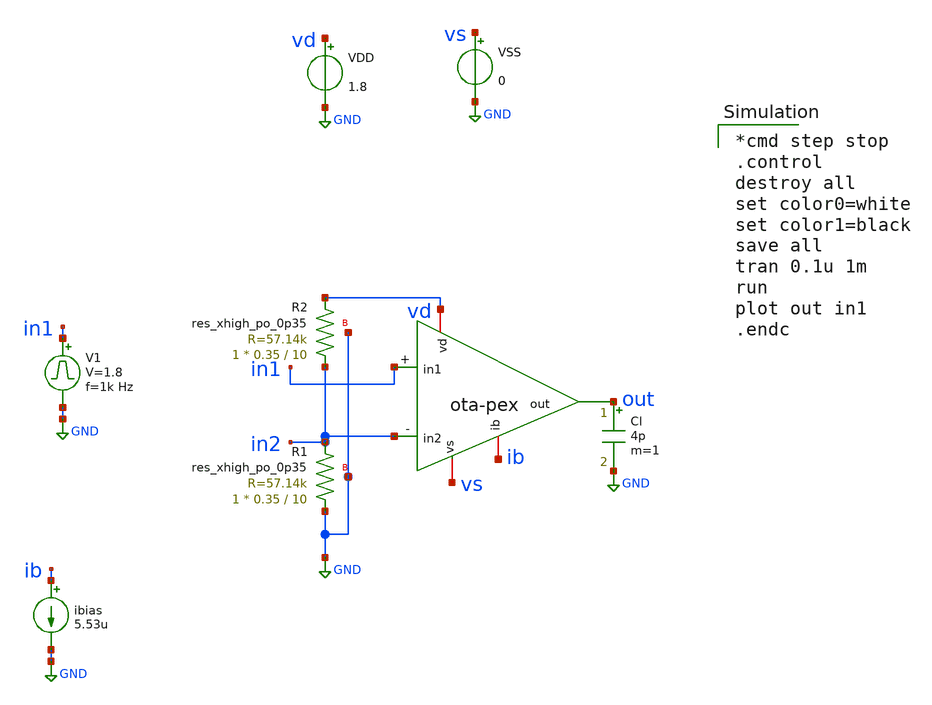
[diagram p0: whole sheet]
** sch_path: ota/xschem/ota_tb-largesignal.sch
* Copyright 2020 Stefan Frederik Schippers
* Licensed under the Apache License, Version 2.0 (the "License");
* you may not use this file except in compliance with the License.
* You may obtain a copy of the License at
* https://www.apache.org/licenses/LICENSE-2.0
* Unless required by applicable law or agreed to in writing, software
* distributed under the License is distributed on an "AS IS" BASIS,
* WITHOUT WARRANTIES OR CONDITIONS OF ANY KIND, either express or implied.
* See the License for the specific language governing permissions and
* limitations under the License.
**.subckt ota_tb-largesignal
ibias ib GND 5.53u
VDD vd GND 1.8
VSS vs GND 0
V1 in1 GND pulse 0 1.8 '0.495/ 1k ' '0.01/1k ' '0.01/1k ' '0.49/1k ' '1/1k '
Cl out GND 4p m=1
XR1 GND in2 GND sky130_fd_pr__res_xhigh_po_0p35 L=10 mult=1 m=1
XR2 in2 vd GND sky130_fd_pr__res_xhigh_po_0p35 L=10 mult=1 m=1
X1 vd ib out in2 in1 vs ota-pex
**** begin user architecture code

*cmd step stop
.control
destroy all
set color0=white
set color1=black
save all
tran 0.1u 1m
run
plot out in1
.endc

 .lib $::SKYWATER_MODELS/sky130.lib.spice tt
.include $::SKYWATER_STDCELLS/sky130_fd_sc_hd.spice

**** end user architecture code
**.ends
.GLOBAL GND
.end
